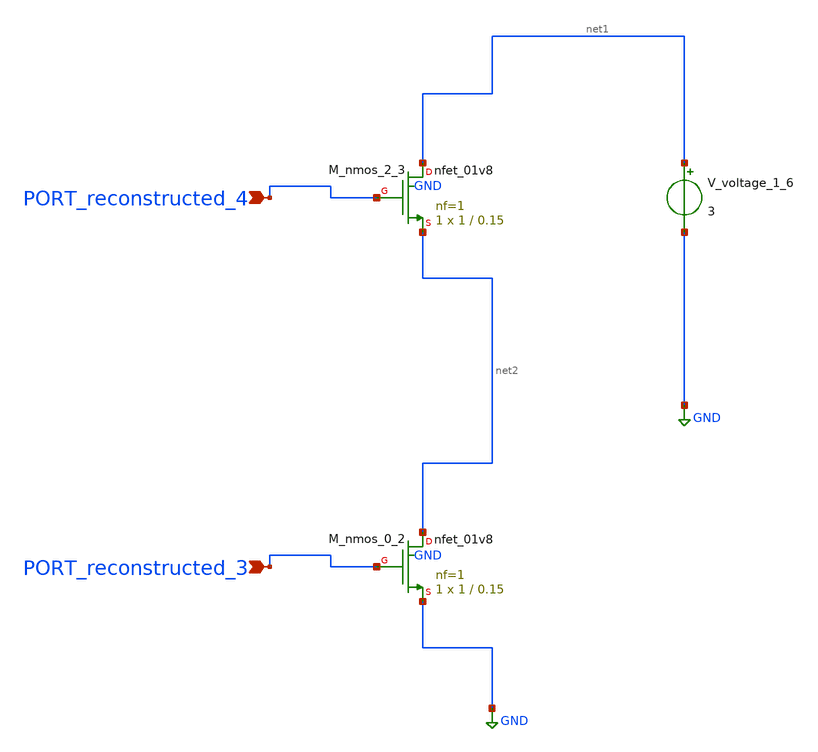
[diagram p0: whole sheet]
** sch_path: schematics/AMSNet/139.sch
**.subckt 139 PORT_reconstructed_3 PORT_reconstructed_4
*.ipin PORT_reconstructed_3
*.ipin PORT_reconstructed_4
XM_nmos_0_2 net2 PORT_reconstructed_3 GND GND sky130_fd_pr__nfet_01v8 L=0.15 W=1 nf=1 ad='int((1 + 1)/2) * 1 / 1 * 0.29'
+ as='int((1 + 2)/2) * 1 / 1 * 0.29' pd='2*int((1 + 1)/2) * (1 / 1 + 0.29)' ps='2*int((1 + 2)/2) * (1 / 1 + 0.29)'
+ nrd='0.29 / 1 ' nrs='0.29 / 1 ' sa=0 sb=0 sd=0 mult=1 m=1
XM_nmos_2_3 net1 PORT_reconstructed_4 net2 GND sky130_fd_pr__nfet_01v8 L=0.15 W=1 nf=1 ad='int((1 + 1)/2) * 1 / 1 * 0.29'
+ as='int((1 + 2)/2) * 1 / 1 * 0.29' pd='2*int((1 + 1)/2) * (1 / 1 + 0.29)' ps='2*int((1 + 2)/2) * (1 / 1 + 0.29)'
+ nrd='0.29 / 1 ' nrs='0.29 / 1 ' sa=0 sb=0 sd=0 mult=1 m=1
V_voltage_1_6 net1 GND 3
**.ends
.GLOBAL GND
.end
